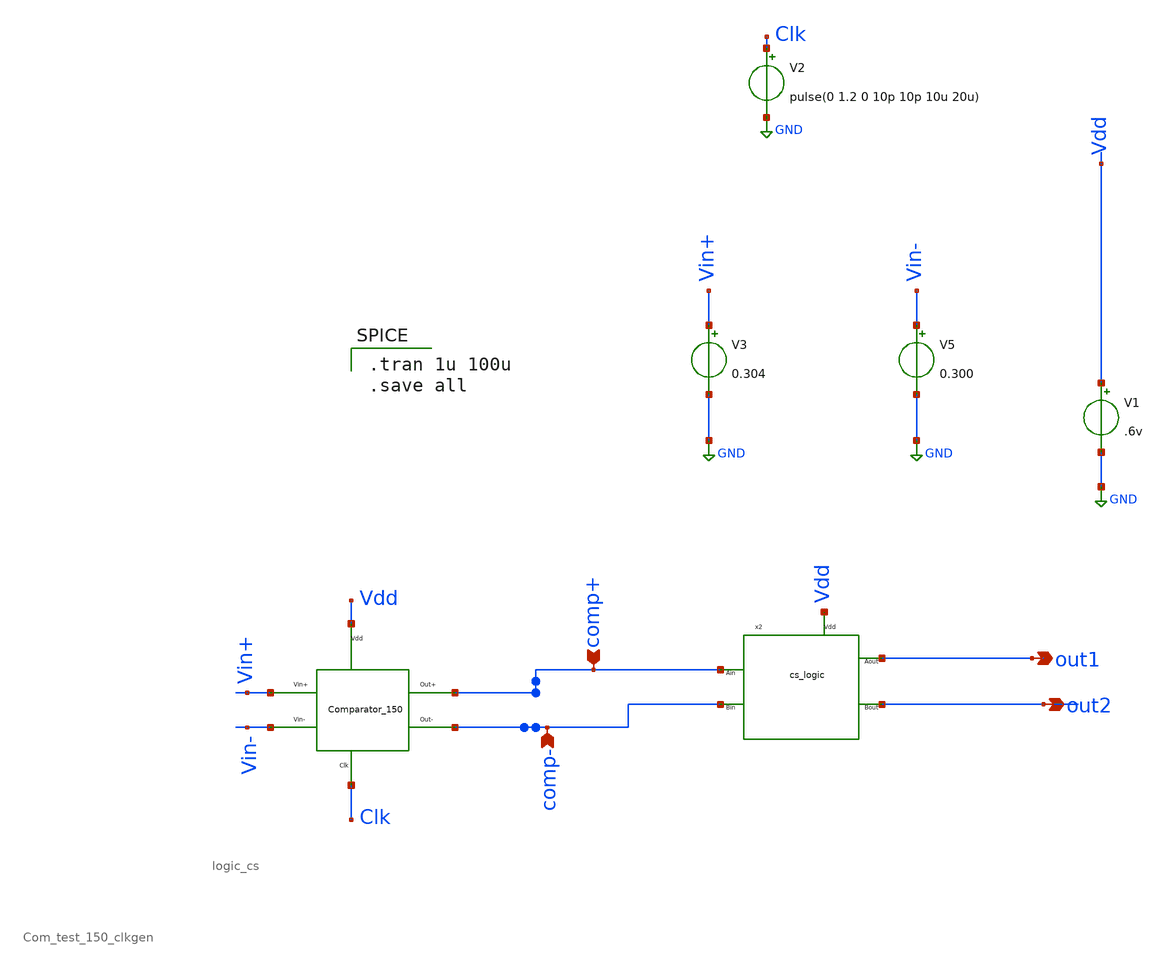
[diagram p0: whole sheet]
** sch_path: Blocks/comparator_150nm/Com_test_150_test.sch
**.subckt Com_test_150_test out1 out2 comp+ comp-
*.opin out1
*.opin out2
*.ipin comp+
*.ipin comp-
V3 Vin+ GND 0.304
V5 Vin- GND 0.300
V1 Vdd GND .6v
V2 Clk GND pulse(0 1.2 0 10p 10p 10u 20u)
x1 Vin+ Vin- comp+ comp- Clk Vdd Com_test_150_clkgen
x2 Vdd out1 out2 comp- comp+ logic_cs
**** begin user architecture code

** opencircuitdesign pdks install
.lib $::SKYWATER_MODELS/sky130.lib.spice tt



.tran 1u 100u
.save all

**** end user architecture code
**.ends

* expanding   symbol:  Blocks/comparator_150nm/Com_test_150_clkgen.sym # of pins=6
** sym_path: Blocks/comparator_150nm/Com_test_150_clkgen.sym
** sch_path: Blocks/comparator_150nm/Com_test_150_clkgen.sch
.subckt Com_test_150_clkgen Vin+ Vin- Out+ Out- Clk Vdd
*.iopin Vin+
*.iopin Vin-
*.iopin Out+
*.iopin Out-
*.ipin Vdd
*.ipin Clk
XM6 net1 Clkb1 Vdd Vdd sky130_fd_pr__pfet_01v8 L=0.15 W=1.26 nf=1 ad='int((nf+1)/2) * W/nf * 0.29' as='int((nf+2)/2) * W/nf * 0.29'
+ pd='2*int((nf+1)/2) * (W/nf + 0.29)' ps='2*int((nf+2)/2) * (W/nf + 0.29)' nrd='0.29 / W' nrs='0.29 / W'
+ sa=0 sb=0 sd=0 mult=1 m=1
XM7 O1- Vin+ net1 Vdd sky130_fd_pr__pfet_01v8 L=0.15 W=1.26 nf=1 ad='int((nf+1)/2) * W/nf * 0.29' as='int((nf+2)/2) * W/nf * 0.29'
+ pd='2*int((nf+1)/2) * (W/nf + 0.29)' ps='2*int((nf+2)/2) * (W/nf + 0.29)' nrd='0.29 / W' nrs='0.29 / W'
+ sa=0 sb=0 sd=0 mult=1 m=1
XM8 O1+ Vin- net1 Vdd sky130_fd_pr__pfet_01v8 L=0.15 W=1.26 nf=1 ad='int((nf+1)/2) * W/nf * 0.29' as='int((nf+2)/2) * W/nf * 0.29'
+ pd='2*int((nf+1)/2) * (W/nf + 0.29)' ps='2*int((nf+2)/2) * (W/nf + 0.29)' nrd='0.29 / W' nrs='0.29 / W'
+ sa=0 sb=0 sd=0 mult=1 m=1
XM9 net5 Clkb2 Vdd Vdd sky130_fd_pr__pfet_01v8 L=0.15 W=1.26 nf=1 ad='int((nf+1)/2) * W/nf * 0.29' as='int((nf+2)/2) * W/nf * 0.29'
+ pd='2*int((nf+1)/2) * (W/nf + 0.29)' ps='2*int((nf+2)/2) * (W/nf + 0.29)' nrd='0.29 / W' nrs='0.29 / W'
+ sa=0 sb=0 sd=0 mult=1 m=1
XM10 net7 Out- net5 Vdd sky130_fd_pr__pfet_01v8 L=0.15 W=1.26 nf=1 ad='int((nf+1)/2) * W/nf * 0.29' as='int((nf+2)/2) * W/nf * 0.29'
+ pd='2*int((nf+1)/2) * (W/nf + 0.29)' ps='2*int((nf+2)/2) * (W/nf + 0.29)' nrd='0.29 / W' nrs='0.29 / W'
+ sa=0 sb=0 sd=0 mult=1 m=1
XM11 Out- O1- net6 Vdd sky130_fd_pr__pfet_01v8 L=0.15 W=1.26 nf=1 ad='int((nf+1)/2) * W/nf * 0.29' as='int((nf+2)/2) * W/nf * 0.29'
+ pd='2*int((nf+1)/2) * (W/nf + 0.29)' ps='2*int((nf+2)/2) * (W/nf + 0.29)' nrd='0.29 / W' nrs='0.29 / W'
+ sa=0 sb=0 sd=0 mult=1 m=1
XM12 Out+ O1+ net7 Vdd sky130_fd_pr__pfet_01v8 L=0.15 W=1.26 nf=1 ad='int((nf+1)/2) * W/nf * 0.29' as='int((nf+2)/2) * W/nf * 0.29'
+ pd='2*int((nf+1)/2) * (W/nf + 0.29)' ps='2*int((nf+2)/2) * (W/nf + 0.29)' nrd='0.29 / W' nrs='0.29 / W'
+ sa=0 sb=0 sd=0 mult=1 m=1
XM13 net6 Out+ net5 Vdd sky130_fd_pr__pfet_01v8 L=0.15 W=1.26 nf=1 ad='int((nf+1)/2) * W/nf * 0.29' as='int((nf+2)/2) * W/nf * 0.29'
+ pd='2*int((nf+1)/2) * (W/nf + 0.29)' ps='2*int((nf+2)/2) * (W/nf + 0.29)' nrd='0.29 / W' nrs='0.29 / W'
+ sa=0 sb=0 sd=0 mult=1 m=1
XM1 O1+ O1- net2 GND sky130_fd_pr__nfet_01v8 L=0.15 W=0.42 nf=1 ad='int((nf+1)/2) * W/nf * 0.29' as='int((nf+2)/2) * W/nf * 0.29'
+ pd='2*int((nf+1)/2) * (W/nf + 0.29)' ps='2*int((nf+2)/2) * (W/nf + 0.29)' nrd='0.29 / W' nrs='0.29 / W'
+ sa=0 sb=0 sd=0 mult=1 m=1
XM3 net2 Vdd GND GND sky130_fd_pr__nfet_01v8 L=0.15 W=0.42 nf=1 ad='int((nf+1)/2) * W/nf * 0.29' as='int((nf+2)/2) * W/nf * 0.29'
+ pd='2*int((nf+1)/2) * (W/nf + 0.29)' ps='2*int((nf+2)/2) * (W/nf + 0.29)' nrd='0.29 / W' nrs='0.29 / W'
+ sa=0 sb=0 sd=0 mult=1 m=1
XM4 O1- O1+ net2 GND sky130_fd_pr__nfet_01v8 L=0.15 W=0.42 nf=1 ad='int((nf+1)/2) * W/nf * 0.29' as='int((nf+2)/2) * W/nf * 0.29'
+ pd='2*int((nf+1)/2) * (W/nf + 0.29)' ps='2*int((nf+2)/2) * (W/nf + 0.29)' nrd='0.29 / W' nrs='0.29 / W'
+ sa=0 sb=0 sd=0 mult=1 m=1
XM5 O1- Clk GND GND sky130_fd_pr__nfet_01v8 L=0.15 W=0.42 nf=1 ad='int((nf+1)/2) * W/nf * 0.29' as='int((nf+2)/2) * W/nf * 0.29'
+ pd='2*int((nf+1)/2) * (W/nf + 0.29)' ps='2*int((nf+2)/2) * (W/nf + 0.29)' nrd='0.29 / W' nrs='0.29 / W'
+ sa=0 sb=0 sd=0 mult=1 m=1
XM21 O1+ Clk GND GND sky130_fd_pr__nfet_01v8 L=0.15 W=0.42 nf=1 ad='int((nf+1)/2) * W/nf * 0.29' as='int((nf+2)/2) * W/nf * 0.29'
+ pd='2*int((nf+1)/2) * (W/nf + 0.29)' ps='2*int((nf+2)/2) * (W/nf + 0.29)' nrd='0.29 / W' nrs='0.29 / W'
+ sa=0 sb=0 sd=0 mult=1 m=1
XM2 Out- Out+ GND GND sky130_fd_pr__nfet_01v8 L=0.15 W=0.42 nf=1 ad='int((nf+1)/2) * W/nf * 0.29' as='int((nf+2)/2) * W/nf * 0.29'
+ pd='2*int((nf+1)/2) * (W/nf + 0.29)' ps='2*int((nf+2)/2) * (W/nf + 0.29)' nrd='0.29 / W' nrs='0.29 / W'
+ sa=0 sb=0 sd=0 mult=1 m=1
XM14 Out+ Clk GND GND sky130_fd_pr__nfet_01v8 L=0.15 W=0.42 nf=1 ad='int((nf+1)/2) * W/nf * 0.29' as='int((nf+2)/2) * W/nf * 0.29'
+ pd='2*int((nf+1)/2) * (W/nf + 0.29)' ps='2*int((nf+2)/2) * (W/nf + 0.29)' nrd='0.29 / W' nrs='0.29 / W'
+ sa=0 sb=0 sd=0 mult=1 m=1
XM15 Out+ Out- GND GND sky130_fd_pr__nfet_01v8 L=0.15 W=0.42 nf=1 ad='int((nf+1)/2) * W/nf * 0.29' as='int((nf+2)/2) * W/nf * 0.29'
+ pd='2*int((nf+1)/2) * (W/nf + 0.29)' ps='2*int((nf+2)/2) * (W/nf + 0.29)' nrd='0.29 / W' nrs='0.29 / W'
+ sa=0 sb=0 sd=0 mult=1 m=1
XM16 Out- Clk GND GND sky130_fd_pr__nfet_01v8 L=0.15 W=0.42 nf=1 ad='int((nf+1)/2) * W/nf * 0.29' as='int((nf+2)/2) * W/nf * 0.29'
+ pd='2*int((nf+1)/2) * (W/nf + 0.29)' ps='2*int((nf+2)/2) * (W/nf + 0.29)' nrd='0.29 / W' nrs='0.29 / W'
+ sa=0 sb=0 sd=0 mult=1 m=1
XM17 net8 Clk GND GND sky130_fd_pr__nfet_01v8 L=0.15 W=0.42 nf=1 ad='int((nf+1)/2) * W/nf * 0.29' as='int((nf+2)/2) * W/nf * 0.29'
+ pd='2*int((nf+1)/2) * (W/nf + 0.29)' ps='2*int((nf+2)/2) * (W/nf + 0.29)' nrd='0.29 / W' nrs='0.29 / W'
+ sa=0 sb=0 sd=0 mult=1 m=1
XM18 net8 Inv GND GND sky130_fd_pr__nfet_01v8 L=0.15 W=0.42 nf=1 ad='int((nf+1)/2) * W/nf * 0.29' as='int((nf+2)/2) * W/nf * 0.29'
+ pd='2*int((nf+1)/2) * (W/nf + 0.29)' ps='2*int((nf+2)/2) * (W/nf + 0.29)' nrd='0.29 / W' nrs='0.29 / W'
+ sa=0 sb=0 sd=0 mult=1 m=1
XM19 net9 Inv Vdd Vdd sky130_fd_pr__pfet_01v8 L=0.15 W=1.26 nf=1 ad='int((nf+1)/2) * W/nf * 0.29' as='int((nf+2)/2) * W/nf * 0.29'
+ pd='2*int((nf+1)/2) * (W/nf + 0.29)' ps='2*int((nf+2)/2) * (W/nf + 0.29)' nrd='0.29 / W' nrs='0.29 / W'
+ sa=0 sb=0 sd=0 mult=1 m=1
XM22 net8 Clk net9 Vdd sky130_fd_pr__pfet_01v8 L=0.15 W=1.26 nf=1 ad='int((nf+1)/2) * W/nf * 0.29' as='int((nf+2)/2) * W/nf * 0.29'
+ pd='2*int((nf+1)/2) * (W/nf + 0.29)' ps='2*int((nf+2)/2) * (W/nf + 0.29)' nrd='0.29 / W' nrs='0.29 / W'
+ sa=0 sb=0 sd=0 mult=1 m=1
x1 net10 net11 Vdd GND black_inv
x2 Clk net10 Vdd GND black_inv
x3 net11 net12 Vdd GND black_inv
x4 net12 net13 Vdd GND black_inv
x6 net13 Inv Vdd GND black_inv
x7 Inv net3 Vdd GND INV
x8 net3 net4 Vdd GND INV
x9 net4 Clkb2 Vdd GND INV
x16 net8 Clkb1 Vdd GND INV
.ends


* expanding   symbol:  Blocks/logic_current_source/logic_cs.sym # of pins=5
** sym_path: Blocks/logic_current_source/logic_cs.sym
** sch_path: Blocks/logic_current_source/logic_cs.sch
.subckt logic_cs Vdd Aout Bout Bin Ain
*.iopin Vdd
*.iopin Aout
*.iopin Bin
*.iopin Ain
*.iopin Bout
x3 Bin net1 Aout Vdd GND NAND
x4 Ain net1 Vdd GND INV
XM1 Bout Bin GND GND sky130_fd_pr__nfet_01v8 L=0.15 W=0.42 nf=1 ad='int((nf+1)/2) * W/nf * 0.29' as='int((nf+2)/2) * W/nf * 0.29'
+ pd='2*int((nf+1)/2) * (W/nf + 0.29)' ps='2*int((nf+2)/2) * (W/nf + 0.29)' nrd='0.29 / W' nrs='0.29 / W'
+ sa=0 sb=0 sd=0 mult=1 m=1
XM2 Bout net1 GND GND sky130_fd_pr__nfet_01v8 L=0.15 W=0.42 nf=1 ad='int((nf+1)/2) * W/nf * 0.29' as='int((nf+2)/2) * W/nf * 0.29'
+ pd='2*int((nf+1)/2) * (W/nf + 0.29)' ps='2*int((nf+2)/2) * (W/nf + 0.29)' nrd='0.29 / W' nrs='0.29 / W'
+ sa=0 sb=0 sd=0 mult=1 m=1
XM3 Bout Bin net2 Vdd sky130_fd_pr__pfet_01v8 L=0.15 W=2.52 nf=1 ad='int((nf+1)/2) * W/nf * 0.29' as='int((nf+2)/2) * W/nf * 0.29'
+ pd='2*int((nf+1)/2) * (W/nf + 0.29)' ps='2*int((nf+2)/2) * (W/nf + 0.29)' nrd='0.29 / W' nrs='0.29 / W'
+ sa=0 sb=0 sd=0 mult=1 m=1
XM4 net2 net1 Vdd Vdd sky130_fd_pr__pfet_01v8 L=0.15 W=2.52 nf=1 ad='int((nf+1)/2) * W/nf * 0.29' as='int((nf+2)/2) * W/nf * 0.29'
+ pd='2*int((nf+1)/2) * (W/nf + 0.29)' ps='2*int((nf+2)/2) * (W/nf + 0.29)' nrd='0.29 / W' nrs='0.29 / W'
+ sa=0 sb=0 sd=0 mult=1 m=1
.ends


* expanding   symbol:  component/black_inv_1/black_inv.sym # of pins=4
** sym_path: component/black_inv_1/black_inv.sym
** sch_path: component/black_inv_1/black_inv.sch
.subckt black_inv X Y VP VN
*.ipin X
*.opin Y
*.iopin VN
*.iopin VP
XM8 Y X VP VP sky130_fd_pr__pfet_01v8 L=.18 W=1.59 nf=1 ad='int((nf+1)/2) * W/nf * 0.29' as='int((nf+2)/2) * W/nf * 0.29'
+ pd='2*int((nf+1)/2) * (W/nf + 0.29)' ps='2*int((nf+2)/2) * (W/nf + 0.29)' nrd='0.29 / W' nrs='0.29 / W'
+ sa=0 sb=0 sd=0 mult=1 m=1
XM4 Y X VN VN sky130_fd_pr__nfet_01v8 L=0.18 W=0.502 nf=1 ad='int((nf+1)/2) * W/nf * 0.29' as='int((nf+2)/2) * W/nf * 0.29'
+ pd='2*int((nf+1)/2) * (W/nf + 0.29)' ps='2*int((nf+2)/2) * (W/nf + 0.29)' nrd='0.29 / W' nrs='0.29 / W'
+ sa=0 sb=0 sd=0 mult=1 m=1
.ends


* expanding   symbol:  component/Inverter/INV.sym # of pins=4
** sym_path: component/Inverter/INV.sym
** sch_path: component/Inverter/INV.sch
.subckt INV X Y VP VN
*.ipin X
*.opin Y
*.iopin VN
*.iopin VP
XM8 Y X VP VP sky130_fd_pr__pfet_01v8 L=.18 W=1.512 nf=1 ad='int((nf+1)/2) * W/nf * 0.29' as='int((nf+2)/2) * W/nf * 0.29'
+ pd='2*int((nf+1)/2) * (W/nf + 0.29)' ps='2*int((nf+2)/2) * (W/nf + 0.29)' nrd='0.29 / W' nrs='0.29 / W'
+ sa=0 sb=0 sd=0 mult=1 m=1
XM4 Y X VN VN sky130_fd_pr__nfet_01v8 L=0.18 W=0.42 nf=1 ad='int((nf+1)/2) * W/nf * 0.29' as='int((nf+2)/2) * W/nf * 0.29'
+ pd='2*int((nf+1)/2) * (W/nf + 0.29)' ps='2*int((nf+2)/2) * (W/nf + 0.29)' nrd='0.29 / W' nrs='0.29 / W'
+ sa=0 sb=0 sd=0 mult=1 m=1
.ends


* expanding   symbol:  component/NAND2/NAND.sym # of pins=5
** sym_path: component/NAND2/NAND.sym
** sch_path: component/NAND2/NAND.sch
.subckt NAND B A Y VP VN
*.iopin VP
*.ipin A
*.ipin B
*.opin Y
*.iopin VN
XM1 Y A VP VP sky130_fd_pr__pfet_01v8 L=0.15 W=1.26 nf=1 ad='int((nf+1)/2) * W/nf * 0.29' as='int((nf+2)/2) * W/nf * 0.29'
+ pd='2*int((nf+1)/2) * (W/nf + 0.29)' ps='2*int((nf+2)/2) * (W/nf + 0.29)' nrd='0.29 / W' nrs='0.29 / W'
+ sa=0 sb=0 sd=0 mult=1 m=1
XM2 Y B VP VP sky130_fd_pr__pfet_01v8 L=0.15 W=1.26 nf=1 ad='int((nf+1)/2) * W/nf * 0.29' as='int((nf+2)/2) * W/nf * 0.29'
+ pd='2*int((nf+1)/2) * (W/nf + 0.29)' ps='2*int((nf+2)/2) * (W/nf + 0.29)' nrd='0.29 / W' nrs='0.29 / W'
+ sa=0 sb=0 sd=0 mult=1 m=1
XM3 Y A net1 net1 sky130_fd_pr__nfet_01v8 L=0.15 W=0.84 nf=1 ad='int((nf+1)/2) * W/nf * 0.29' as='int((nf+2)/2) * W/nf * 0.29'
+ pd='2*int((nf+1)/2) * (W/nf + 0.29)' ps='2*int((nf+2)/2) * (W/nf + 0.29)' nrd='0.29 / W' nrs='0.29 / W'
+ sa=0 sb=0 sd=0 mult=1 m=1
XM4 net1 B VN VN sky130_fd_pr__nfet_01v8 L=0.15 W=0.84 nf=1 ad='int((nf+1)/2) * W/nf * 0.29' as='int((nf+2)/2) * W/nf * 0.29'
+ pd='2*int((nf+1)/2) * (W/nf + 0.29)' ps='2*int((nf+2)/2) * (W/nf + 0.29)' nrd='0.29 / W' nrs='0.29 / W'
+ sa=0 sb=0 sd=0 mult=1 m=1
.ends

.GLOBAL GND
.end
